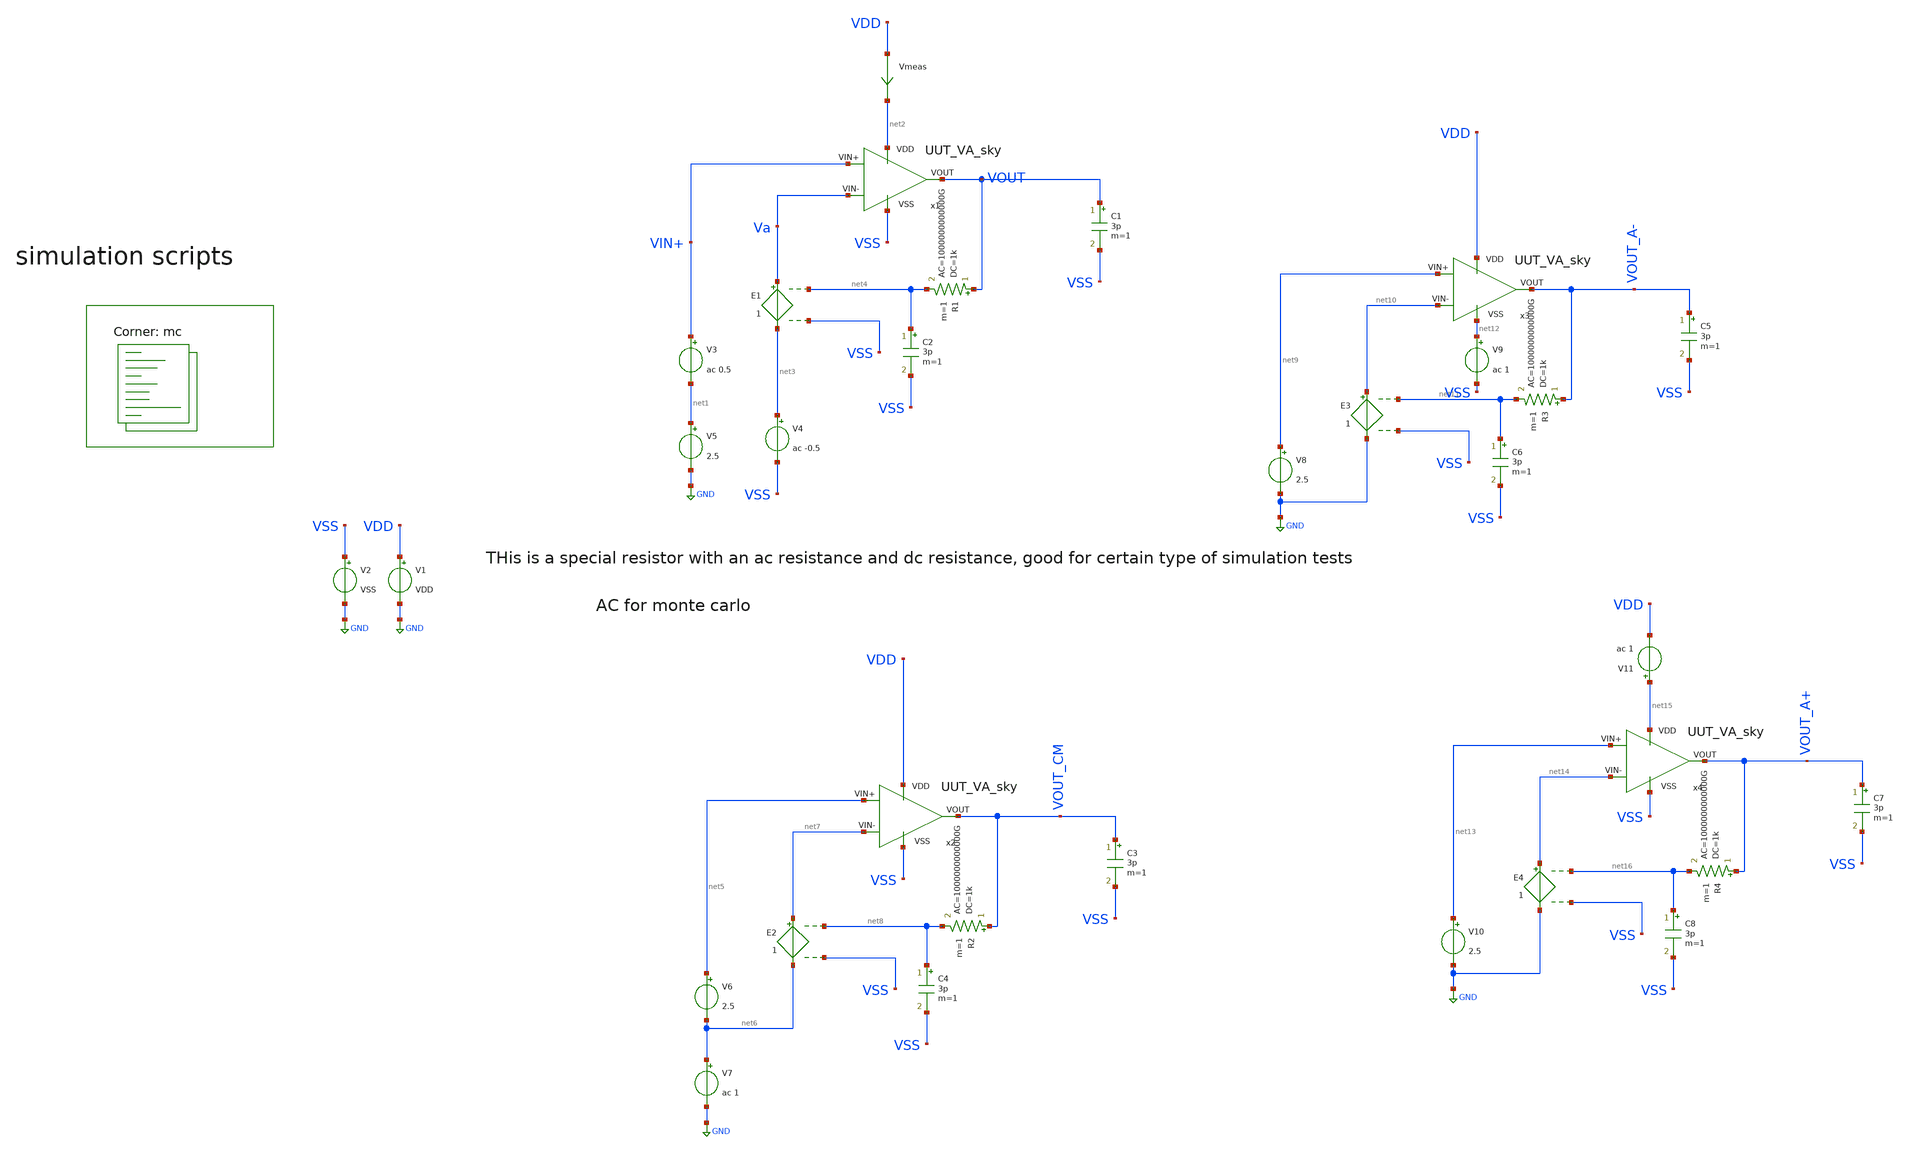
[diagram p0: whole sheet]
** sch_path: Learning/single_ended_amplifiers/Design_and_Analysis_of_Two-Stage_CMOS_Operational_Amplifier_for_Fluorescence_Signal_Processing_sky130_5V/amplifier_design/OTA_mc_ac_tb.sch
**.subckt OTA_mc_ac_tb
V1 VDD GND VDD
V2 VSS GND VSS
Vmeas VDD net2 0
.save i(vmeas)
x1 net2 VSS Va VIN+ VOUT UUT_VA_sky
C1 VOUT VSS 3p m=1
V5 net1 GND 2.5
V3 VIN+ net1 ac 0.5
V4 net3 VSS ac -0.5
E1 Va net3 net4 VSS 1
R1 VOUT net4 1k ac=1000000000000G m=1
C2 net4 VSS 3p m=1
x2 VDD VSS net7 net5 VOUT_CM UUT_VA_sky
C3 VOUT_CM VSS 3p m=1
V6 net5 net6 2.5
V7 net6 GND ac 1
E2 net7 net6 net8 VSS 1
R2 VOUT_CM net8 1k ac=1000000000000G m=1
C4 net8 VSS 3p m=1
x3 VDD net12 net10 net9 VOUT_A- UUT_VA_sky
C5 VOUT_A- VSS 3p m=1
V8 net9 GND 2.5
E3 net10 GND net11 VSS 1
R3 VOUT_A- net11 1k ac=1000000000000G m=1
C6 net11 VSS 3p m=1
V9 net12 VSS ac 1
x4 net15 VSS net14 net13 VOUT_A+ UUT_VA_sky
C7 VOUT_A+ VSS 3p m=1
V10 net13 GND 2.5
E4 net14 GND net16 VSS 1
R4 VOUT_A+ net16 1k ac=1000000000000G m=1
C8 net16 VSS 3p m=1
V11 net15 VDD ac 1
**** begin user architecture code
.lib $::SKYWATER_MODELS/sky130.lib.spice mc

.Temp 27
.param VDD = 1.8
.param VSS = 0
.param CL = 3p
.param mc_mm_switch = 1


.control

	save all
	ac dec 100 1 10G
	plot db(v(VOUT))
	plot db(v(VOUT_CM))
	plot db(v(VOUT_A-))
	plot db(v(VOUT_A+))
	wrdata mc_ac.csv db(v(VOUT)) phase(v(VOUT)) db(v(VOUT_CM)) db(v(VOUT_A-)) db(v(VOUT_A+))
.endc

**** end user architecture code
**.ends

* expanding   symbol:  Sky130A/UUT_sky/UUT_VA_sky.sym # of pins=5
** sym_path: my_ip/LIB/Sky130A/UUT_sky/UUT_VA_sky.sym
** sch_path: my_ip/LIB/Sky130A/UUT_sky/UUT_VA_sky.sch
.subckt UUT_VA_sky VDD VSS VIN- VIN+ VOUT
*.iopin VDD
*.iopin VSS
*.iopin VIN-
*.iopin VIN+
*.iopin VOUT
x1 VDD VSS VIN+ VIN- VOUT A001
.ends

.GLOBAL GND
.end
